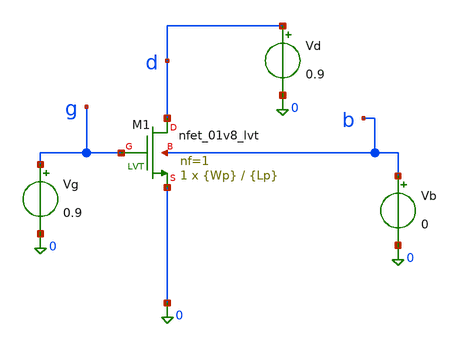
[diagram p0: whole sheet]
** sch_path: parameter_extraction/nmos_lvt_characterization.sch
**.subckt nmos_lvt_characterization
XM1 d g 0 b sky130_fd_pr__nfet_01v8_lvt L={Lp} W={Wp} nf=1 ad='int((1 + 1)/2) * {Wp} / 1 * 0.29' as='int((1 + 2)/2) * {Wp} / 1 * 0.29'
+ pd='2*int((1 + 1)/2) * ({Wp} / 1 + 0.29)' ps='2*int((1 + 2)/2) * ({Wp} / 1 + 0.29)' nrd='0.29 / {Wp} '
+ nrs='0.29 / {Wp} ' sa=0 sb=0 sd=0 mult=1 m=1
Vg g 0 0.9
Vb b 0 0
Vd d 0 0.9
**** begin user architecture code


.lib /foss/pdks/sky130A/libs.tech/combined/sky130.lib.spice tt
.param Lp=0.6 Wp=5
.save all @m.xm1.msky130_fd_pr__nfet_01v8_lvt[vth]

.control
set llist = ( 0.6 0.7 0.8 0.9 1.0 )
let W    = 5
let vov  = 0.2
let vgsb = 0.9
set color0=white
set xbrushwidth=2
set p_sq  = ( )
set p_kp  = ( )
set p_vth = ( )
set p_gmid = ( )
set p_lam = ( )
set p_id  = ( )
set p_vsb = ( )

foreach lv $llist
  alterparam Lp = $lv
  reset
  alter Vd dc=0.9
  alter Vb dc=0
  dc Vg 0 1.8 0.005
  let id     = -i(Vd)
  let sqrtid = sqrt(id)
  let vth    = @m.xm1.msky130_fd_pr__nfet_01v8_lvt[vth]
  let kp     = 2*deriv(sqrtid)^2*$lv/W*1e6
  let gmid   = deriv(id)/id
  let vth_op = vth[160]
  set p_sq   = ( $p_sq {$curplot}.sqrtid )
  set p_kp   = ( $p_kp {$curplot}.kp )
  set p_vth  = ( $p_vth {$curplot}.vth )
  set p_gmid = ( $p_gmid {$curplot}.gmid )
  echo L = $lv um : model Vth = $&vth_op V

  let vg_out = vth_op + vov
  alter Vg dc=$&vg_out
  dc Vd 0 1.8 0.005
  let id  = -i(Vd)
  let gds = deriv(id)
  let lam = gds/(id - gds*v(d))
  set p_id  = ( $p_id {$curplot}.id )
  set p_lam = ( $p_lam {$curplot}.lam )

  alter Vg dc=$&vgsb
  alter Vd dc=0.9
  dc Vb 0 -0.9 -0.01
  let vth = @m.xm1.msky130_fd_pr__nfet_01v8_lvt[vth]
  set p_vsb = ( $p_vsb {$curplot}.vth )
end

plot $p_sq  xlabel 'VGS (V)' ylabel 'sqrt(ID)' title 'sqrt(ID) vs VGS'
plot $p_kp  xlimit 0.4 1.4 ylimit 0 300 xlabel 'VGS (V)' ylabel 'uCox (uA/V^2)' title 'local uCox'
plot $p_vth xlimit 0.3 1.4 xlabel 'VGS (V)' ylabel 'Vth (V)' title 'model Vth vs VGS'
plot $p_gmid xlimit 0.3 1.4 ylimit 0 30 xlabel 'VGS (V)' ylabel 'gm/ID (1/V)' title 'gm/ID'
plot $p_id  xlabel 'VDS (V)' ylabel 'ID (A)' title 'ID vs VDS at VGS = Vth + vov'
plot $p_lam xlimit 0.3 1.6 ylimit 0 0.3 xlabel 'VDS (V)' ylabel 'lambda (1/V)' title 'lambda vs VDS'
plot $p_vsb xlabel 'VB (V)  (VSB = -VB)' ylabel 'Vth (V)' title 'body effect'
.endc


**** end user architecture code
**.ends
.end
